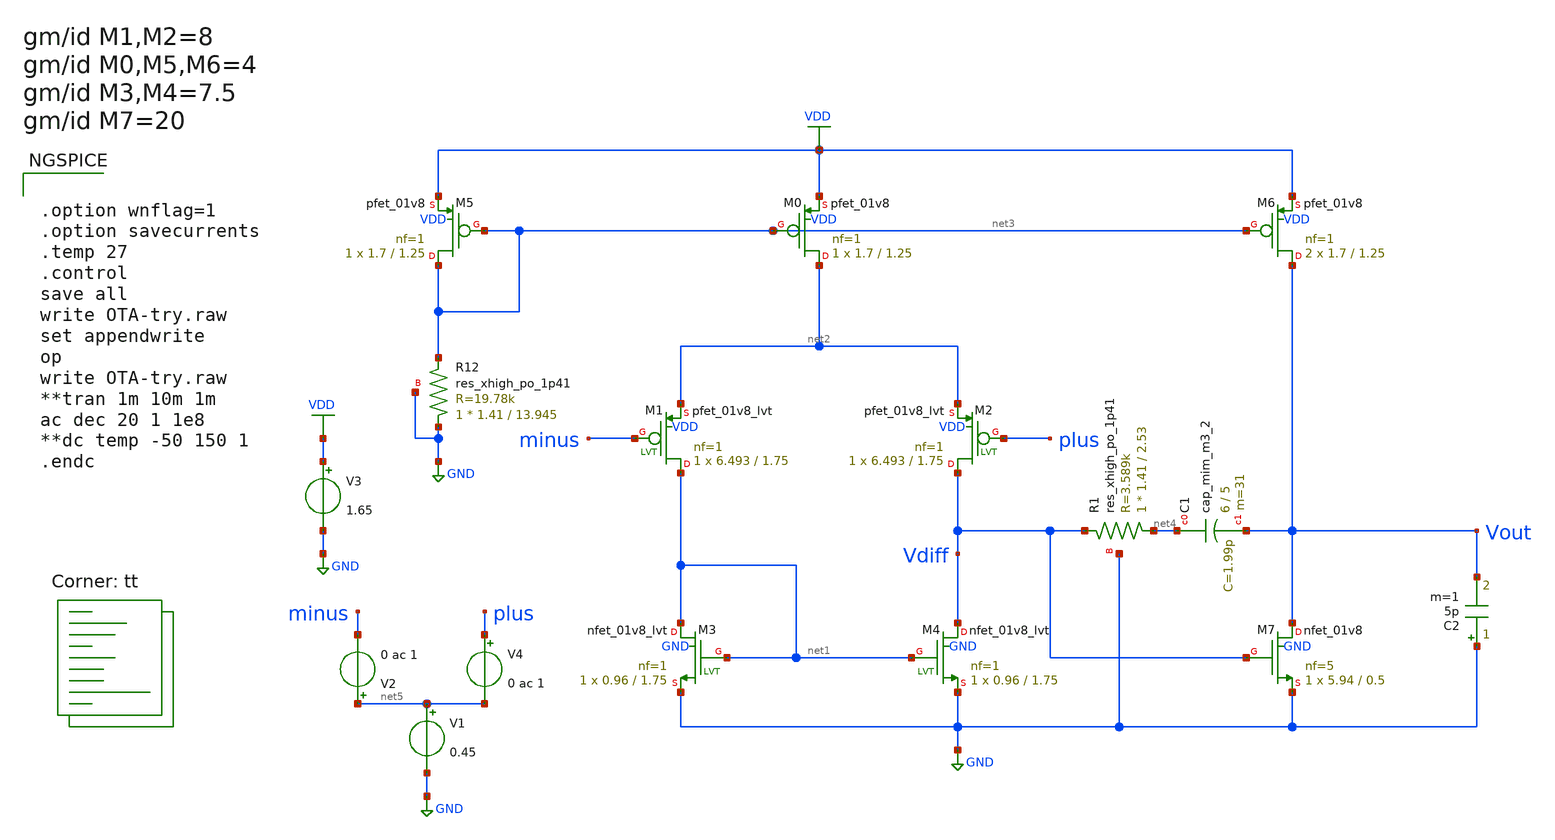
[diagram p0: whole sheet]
** sch_path: Schematic/OTA-try.sch
**.subckt OTA-try
XM3 net1 net1 GND GND sky130_fd_pr__nfet_01v8_lvt L=1.75 W=0.96 nf=1 ad='int((nf+1)/2) * W/nf * 0.29'
+ as='int((nf+2)/2) * W/nf * 0.29' pd='2*int((nf+1)/2) * (W/nf + 0.29)' ps='2*int((nf+2)/2) * (W/nf + 0.29)'
+ nrd='0.29 / W' nrs='0.29 / W' sa=0 sb=0 sd=0 mult=1 m=1
XM1 net1 minus net2 VDD sky130_fd_pr__pfet_01v8_lvt L=1.75 W=6.493 nf=1 ad='int((nf+1)/2) * W/nf * 0.29'
+ as='int((nf+2)/2) * W/nf * 0.29' pd='2*int((nf+1)/2) * (W/nf + 0.29)' ps='2*int((nf+2)/2) * (W/nf + 0.29)'
+ nrd='0.29 / W' nrs='0.29 / W' sa=0 sb=0 sd=0 mult=1 m=1
V1 net5 GND 0.45
V3 VDD GND 1.65
C2 GND Vout 5p m=1
V4 plus net5 0 ac 1
XM4 Vdiff net1 GND GND sky130_fd_pr__nfet_01v8_lvt L=1.75 W=0.96 nf=1 ad='int((nf+1)/2) * W/nf * 0.29'
+ as='int((nf+2)/2) * W/nf * 0.29' pd='2*int((nf+1)/2) * (W/nf + 0.29)' ps='2*int((nf+2)/2) * (W/nf + 0.29)'
+ nrd='0.29 / W' nrs='0.29 / W' sa=0 sb=0 sd=0 mult=1 m=1
XM2 Vdiff plus net2 VDD sky130_fd_pr__pfet_01v8_lvt L=1.75 W=6.493 nf=1 ad='int((nf+1)/2) * W/nf * 0.29'
+ as='int((nf+2)/2) * W/nf * 0.29' pd='2*int((nf+1)/2) * (W/nf + 0.29)' ps='2*int((nf+2)/2) * (W/nf + 0.29)'
+ nrd='0.29 / W' nrs='0.29 / W' sa=0 sb=0 sd=0 mult=1 m=1
XM0 net2 net3 VDD VDD sky130_fd_pr__pfet_01v8 L=1.25 W=1.7 nf=1 ad='int((nf+1)/2) * W/nf * 0.29' as='int((nf+2)/2) * W/nf * 0.29'
+ pd='2*int((nf+1)/2) * (W/nf + 0.29)' ps='2*int((nf+2)/2) * (W/nf + 0.29)' nrd='0.29 / W' nrs='0.29 / W'
+ sa=0 sb=0 sd=0 mult=1 m=1
XM5 net3 net3 VDD VDD sky130_fd_pr__pfet_01v8 L=1.25 W=1.7 nf=1 ad='int((nf+1)/2) * W/nf * 0.29' as='int((nf+2)/2) * W/nf * 0.29'
+ pd='2*int((nf+1)/2) * (W/nf + 0.29)' ps='2*int((nf+2)/2) * (W/nf + 0.29)' nrd='0.29 / W' nrs='0.29 / W'
+ sa=0 sb=0 sd=0 mult=1 m=1
XM6 Vout net3 VDD VDD sky130_fd_pr__pfet_01v8 L=1.25 W=1.7 nf=1 ad='int((nf+1)/2) * W/nf * 0.29' as='int((nf+2)/2) * W/nf * 0.29'
+ pd='2*int((nf+1)/2) * (W/nf + 0.29)' ps='2*int((nf+2)/2) * (W/nf + 0.29)' nrd='0.29 / W' nrs='0.29 / W'
+ sa=0 sb=0 sd=0 mult=2 m=2
V2 net5 minus 0 ac 1
XM7 Vout Vdiff GND GND sky130_fd_pr__nfet_01v8 L=0.5 W=5.94 nf=5 ad='int((nf+1)/2) * W/nf * 0.29' as='int((nf+2)/2) * W/nf * 0.29'
+ pd='2*int((nf+1)/2) * (W/nf + 0.29)' ps='2*int((nf+2)/2) * (W/nf + 0.29)' nrd='0.29 / W' nrs='0.29 / W'
+ sa=0 sb=0 sd=0 mult=1 m=1
XR12 GND net3 GND sky130_fd_pr__res_xhigh_po_1p41 L=13.945 mult=1 m=1
XR1 net4 Vdiff GND sky130_fd_pr__res_xhigh_po_1p41 L=2.53 mult=1 m=1
XC1 net4 Vout sky130_fd_pr__cap_mim_m3_2 W=6 L=5 MF=31 m=31
**** begin user architecture code


.option wnflag=1
.option savecurrents
.temp 27
.control
save all
write OTA-try.raw
set appendwrite
op
write OTA-try.raw
**tran 1m 10m 1m
ac dec 20 1 1e8
**dc temp -50 150 1
.endc


.lib $::SKYWATER_MODELS/sky130.lib.spice tt
**** end user architecture code
**.ends
.GLOBAL GND
.GLOBAL VDD
.end
